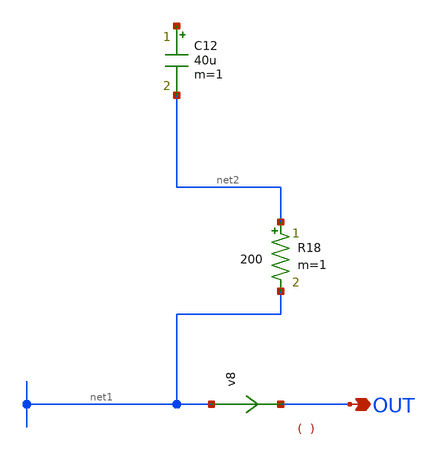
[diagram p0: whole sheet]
** sch_path: tests/from_user/desired_beautified_1.sch
**.subckt desired_beautified_1 OUT
*.opin OUT
C12 net3 net2 40u m=1
R18 net2 net1 200 m=1
v8 net1 OUT 0
.save i(v8)
**.ends
.end
